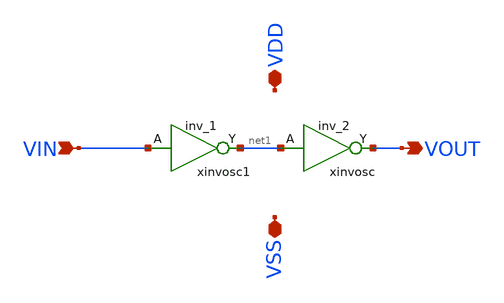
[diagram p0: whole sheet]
** sch_path: modules/BUFFMIN/symbol/BUFFMIN.sch
**.subckt BUFFMIN VDD VSS VIN VOUT
*.iopin VDD
*.iopin VSS
*.ipin VIN
*.opin VOUT
xinvosc net1 VSS VSS VDD VDD VOUT sky130_fd_sc_hd__inv_2
xinvosc1 VIN VSS VSS VDD VDD net1 sky130_fd_sc_hd__inv_1
**.ends
.end
